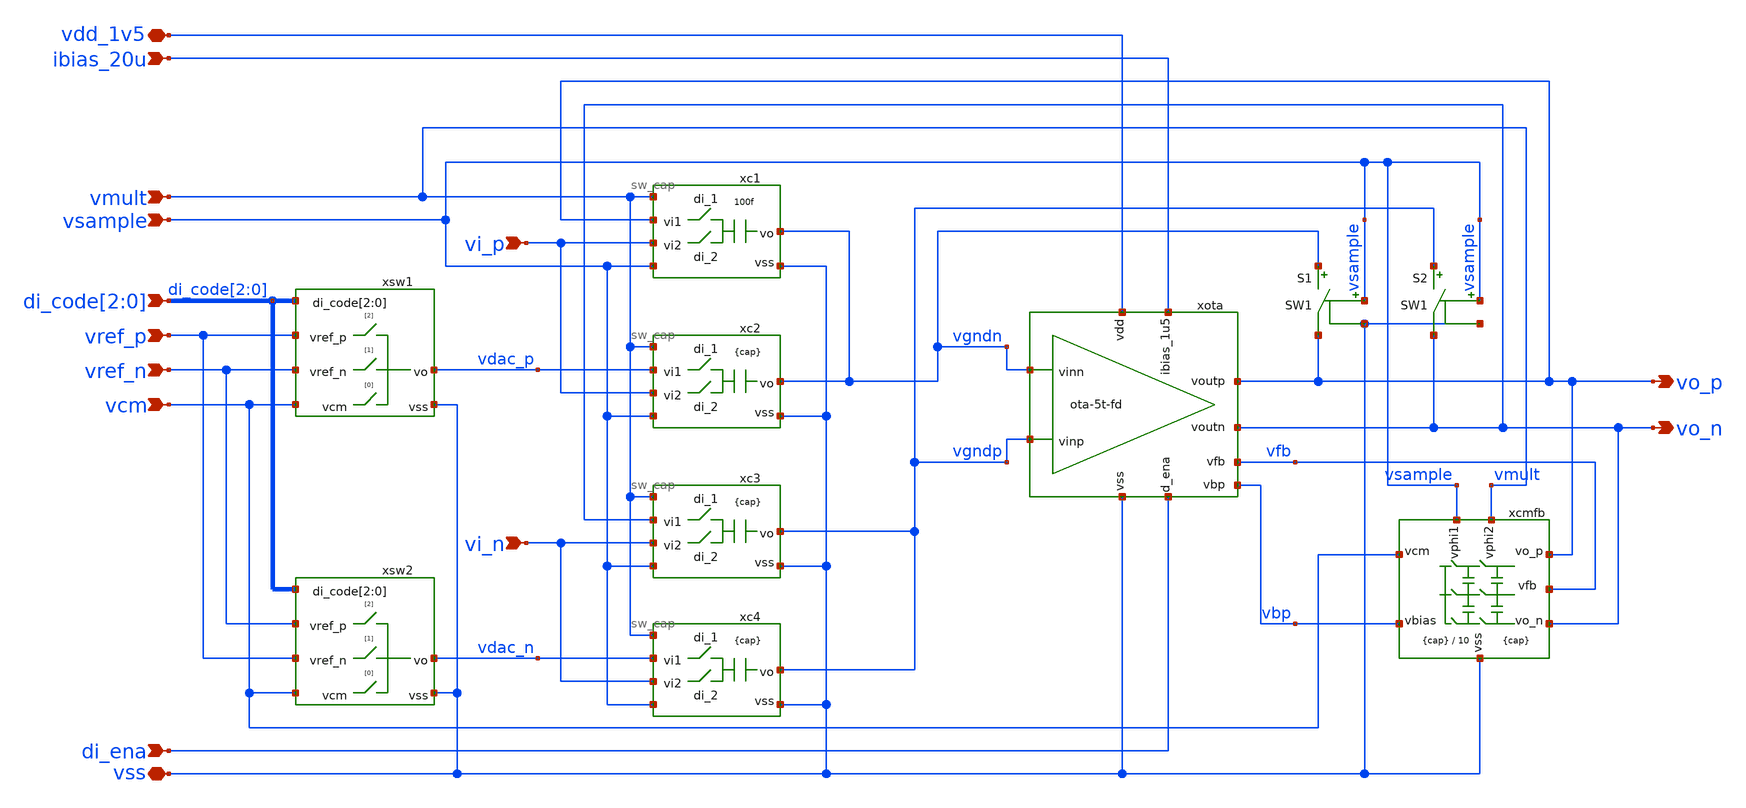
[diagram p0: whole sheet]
** sch_path: xschem/mdac-tri-lvl.sch
* xschem/ota-5t-fd.sch:
* (c) 2025 M. Koefinger
**.subckt mdac-tri-lvl vi_p vi_n di_ena vss vdd_1v5 ibias_20u vo_n vo_p vref_p vref_n vcm
*+ di_code[2],di_code[1],di_code[0] vsample vmult
*.ipin vi_p
*.ipin vi_n
*.ipin di_ena
*.iopin vss
*.iopin vdd_1v5
*.ipin ibias_20u
*.opin vo_n
*.opin vo_p
*.ipin vref_p
*.ipin vref_n
*.ipin vcm
*.ipin di_code[2],di_code[1],di_code[0]
*.ipin vsample
*.ipin vmult
xota vdd_1v5 vfb vo_p vo_n vgndp vgndn ibias_20u di_ena vss vbp ota-5t-fd
S1 vgndn vo_p vsample vss SW1
xcmfb vmult vsample vss vo_p vcm vbp vfb vo_n cmfb_sc cap={cap} div=10
S2 vgndp vo_n vsample vss SW1
xc1 vmult vo_p vgndn vi_p vsample vss sw_cap cap=100f ron=1 roff=1G
xc2 vmult vdac_p vgndn vi_p vsample vss sw_cap cap={cap} ron=1 roff=1G
xc3 vmult vo_n vgndp vi_n vsample vss sw_cap cap={cap} ron=1 roff=1G
xc4 vmult vdac_n vgndp vi_n vsample vss sw_cap cap={cap} ron=1 roff=1G
xsw1 di_code[2] di_code[1] di_code[0] vref_p vref_n vdac_p vcm vss sw_dac ron=1 roff=1G
xsw2 di_code[2] di_code[1] di_code[0] vref_n vref_p vdac_n vcm vss sw_dac ron=1 roff=1G
**.ends

* expanding   symbol:  ota-5t-fd.sym # of pins=10
** sym_path: xschem/ota-5t-fd.sym
** sch_path: xschem/ota-5t-fd.sch
.subckt ota-5t-fd vdd vfb voutp voutn vinp vinn ibias_1u5 d_ena vss vbp
*.ipin ibias_1u5
*.iopin vdd
*.iopin vss
*.ipin vinp
*.ipin vinn
*.opin voutn
*.ipin d_ena
*.opin voutp
*.ipin vfb
*.opin vbp
XMN3 tail gate_n vss vss sg13_lv_nmos w=2.5u l=0.5u ng=5 m=1 mm_ok=1
XMP2 voutp vfb vdd vdd sg13_lv_pmos w=0.5u l=0.5u ng=1 m=1 mm_ok=1
XMN1 voutn vinp tail vss sg13_lv_nmos w=5.5u l=0.5u ng=11 m=1 mm_ok=1
XMN2 voutp vinn tail vss sg13_lv_nmos w=5.5u l=0.5u ng=11 m=1 mm_ok=1
XMP1 voutn vfb vdd vdd sg13_lv_pmos w=0.5u l=0.5u ng=1 m=1 mm_ok=1
XMN4 ibias_1u5 gate_n vss vss sg13_lv_nmos w=1.5u l=0.5u ng=3 m=1 mm_ok=1
XMN5 gate_n ena_n vss vss sg13_lv_nmos w=0.5u l=0.13u ng=1 m=1 mm_ok=1
XMPSW1 vfb ena vdd vdd sg13_lv_pmos w=1.5u l=0.13u ng=1 m=1 mm_ok=1
XMN8 ena ena_n vss vss sg13_lv_nmos w=0.5u l=0.13u ng=1 m=1 mm_ok=1
XMP5 ena ena_n vdd vdd sg13_lv_pmos w=1.5u l=0.13u ng=1 m=1 mm_ok=1
XMN6 ibias_1u5 ena gate_n vss sg13_lv_nmos w=0.5u l=0.13u ng=1 m=1 mm_ok=1
XMN7 ena_n d_ena vss vss sg13_lv_nmos w=0.5u l=0.13u ng=1 m=1 mm_ok=1
XMP4 ena_n d_ena vdd vdd sg13_lv_pmos w=1.5u l=0.13u ng=1 m=1 mm_ok=1
XMN9 vbp gate_n vss vss sg13_lv_nmos w=1u l=0.5u ng=2 m=1 mm_ok=1
XMP3 vbp vbp vdd vdd sg13_lv_pmos w=0.5u l=0.5u ng=1 m=1 mm_ok=1
.ends


* expanding   symbol:  cmfb_sc.sym # of pins=8
** sym_path: xschem/cmfb_sc.sym
** sch_path: xschem/cmfb_sc.sch
.subckt cmfb_sc vphi2 vphi1 vss vo_p vcm vbias vfb vo_n  cap=100f div=10
*.ipin vcm
*.ipin vphi2
*.ipin vphi1
*.iopin vss
*.ipin vbias
*.iopin vo_p
*.iopin vo_n
*.opin vfb
C1 vo_p vfb 100f m=1
C2 net1 net2 10f m=1
C3 vfb vo_n 100f m=1
C4 net2 net3 10f m=1
S3 net1 vo_p vphi1 vss SW1
S4 vcm net1 vphi2 vss SW1
S6 net2 vfb vphi1 vss SW1
S7 vbias net2 vphi2 vss SW1
S9 net3 vo_n vphi1 vss SW1
S10 vcm net3 vphi2 vss SW1
.ends


* expanding   symbol:  sw_cap.sym # of pins=6
** sym_path: xschem/sw_cap.sym
** sch_path: xschem/sw_cap.sch
.subckt sw_cap di_1 vi1 vo vi2 di_2 vss  cap=100f ron=1 roff=1G
*.ipin di_1
*.ipin di_2
*.iopin vi1
*.iopin vi2
*.iopin vo
*.iopin vss
C1 vc_p vo {cap} m=1
S1 vi1 vc_p di_1 vss SW1
S2 vi2 vc_p di_2 vss SW1
.ends


* expanding   symbol:  sw_dac.sym # of pins=6
** sym_path: xschem/sw_dac.sym
** sch_path: xschem/sw_dac.sch
.subckt sw_dac di_code[2] di_code[1] di_code[0] vref_p vref_n vo vcm vss  ron=1 roff=1G
*.ipin di_code[2],di_code[1],di_code[0]
*.iopin vref_p
*.iopin vref_n
*.iopin vo
*.iopin vss
*.iopin vcm
S1 vref_p vo di_code[2] vss SW1
S2 vref_n vo di_code[1] vss SW1
S3 vcm vo di_code[0] vss SW1
.ends

**** begin user architecture code
.MODEL SW1 SW( VT=0.75 VH=0.01 RON=ron ROFF=roff )
**** end user architecture code
.end
